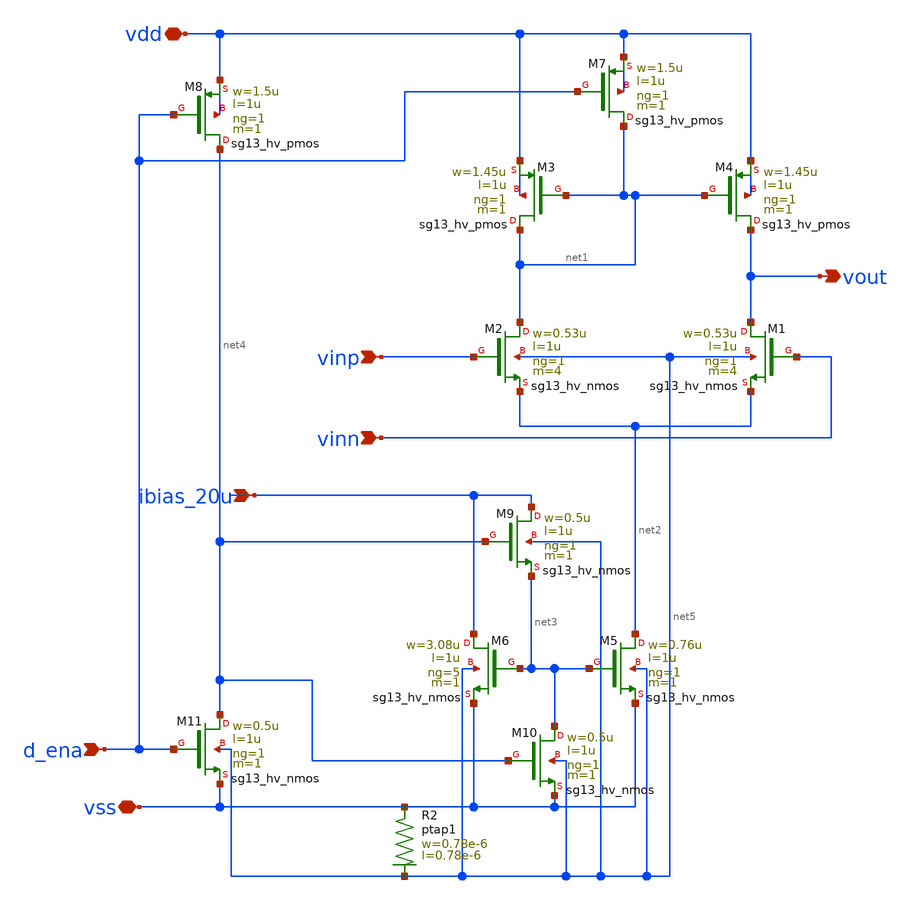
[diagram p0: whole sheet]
** sch_path: Differntial_Amp_50MHz/doc/ota.sch
**.subckt ota vout vdd vss ibias_20u vinn vinp d_ena
*.opin vout
*.iopin vdd
*.iopin vss
*.ipin ibias_20u
*.ipin vinn
*.ipin vinp
*.ipin d_ena
XM1 vout vinn net2 net5 sg13_hv_nmos w=0.53u l=1u ng=1 m=4 mm_ok=1
XM2 net1 vinp net2 net5 sg13_hv_nmos w=0.53u l=1u ng=1 m=4 mm_ok=1
XM5 net2 net3 vss net5 sg13_hv_nmos w=0.76u l=1u ng=1 m=1 mm_ok=1
XM3 net1 net1 vdd vdd sg13_hv_pmos w=1.45u l=1u ng=1 m=1 mm_ok=1
XM4 vout net1 vdd vdd sg13_hv_pmos w=1.45u l=1u ng=1 m=1 mm_ok=1
XM6 ibias_20u net3 vss net5 sg13_hv_nmos w=3.08u l=1u ng=5 m=1 mm_ok=1
XM7 net1 d_ena vdd vdd sg13_hv_pmos w=1.5u l=1u ng=1 m=1 mm_ok=1
XM8 net4 d_ena vdd vdd sg13_hv_pmos w=1.5u l=1u ng=1 m=1 mm_ok=1
XM9 ibias_20u net4 net3 net5 sg13_hv_nmos w=0.5u l=1u ng=1 m=1 mm_ok=1
XM10 net3 net4 vss net5 sg13_hv_nmos w=0.5u l=1u ng=1 m=1 mm_ok=1
XM11 net4 d_ena vss net5 sg13_hv_nmos w=0.5u l=1u ng=1 m=1 mm_ok=1
XR2 vss net5 ptap1 R=262.8 w=0.78e-6 l=0.78e-6
**.ends
.end
